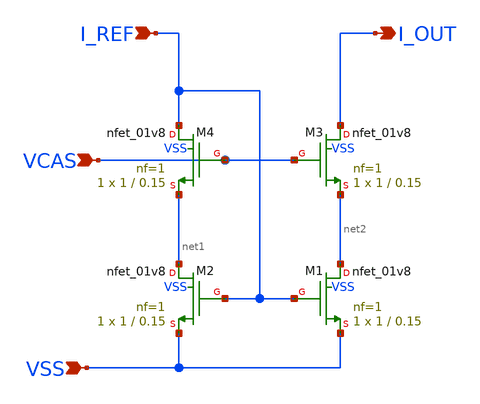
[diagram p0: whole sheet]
** sch_path: designs/analog_library/bias_3.sch
**.subckt bias_3 I_REF I_OUT VSS VCAS
*.ipin I_REF
*.opin I_OUT
*.ipin VSS
*.ipin VCAS
XM1 net2 I_REF VSS VSS sky130_fd_pr__nfet_01v8 L=0.15 W=1 nf=1 ad='int((nf+1)/2) * W/nf * 0.29' as='int((nf+2)/2) * W/nf * 0.29'
+ pd='2*int((nf+1)/2) * (W/nf + 0.29)' ps='2*int((nf+2)/2) * (W/nf + 0.29)' nrd='0.29 / W' nrs='0.29 / W'
+ sa=0 sb=0 sd=0 mult=1 m=1
XM2 net1 I_REF VSS VSS sky130_fd_pr__nfet_01v8 L=0.15 W=1 nf=1 ad='int((nf+1)/2) * W/nf * 0.29' as='int((nf+2)/2) * W/nf * 0.29'
+ pd='2*int((nf+1)/2) * (W/nf + 0.29)' ps='2*int((nf+2)/2) * (W/nf + 0.29)' nrd='0.29 / W' nrs='0.29 / W'
+ sa=0 sb=0 sd=0 mult=1 m=1
XM3 I_OUT VCAS net2 VSS sky130_fd_pr__nfet_01v8 L=0.15 W=1 nf=1 ad='int((nf+1)/2) * W/nf * 0.29' as='int((nf+2)/2) * W/nf * 0.29'
+ pd='2*int((nf+1)/2) * (W/nf + 0.29)' ps='2*int((nf+2)/2) * (W/nf + 0.29)' nrd='0.29 / W' nrs='0.29 / W'
+ sa=0 sb=0 sd=0 mult=1 m=1
XM4 I_REF VCAS net1 VSS sky130_fd_pr__nfet_01v8 L=0.15 W=1 nf=1 ad='int((nf+1)/2) * W/nf * 0.29' as='int((nf+2)/2) * W/nf * 0.29'
+ pd='2*int((nf+1)/2) * (W/nf + 0.29)' ps='2*int((nf+2)/2) * (W/nf + 0.29)' nrd='0.29 / W' nrs='0.29 / W'
+ sa=0 sb=0 sd=0 mult=1 m=1
**.ends
.end
